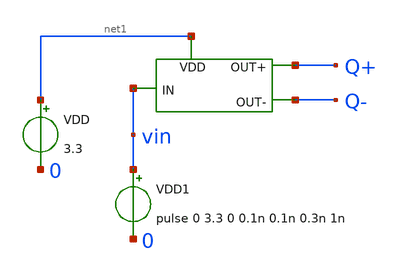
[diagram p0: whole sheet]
** sch_path: initial_notebooks_2023/Current-Steering DAC/DAC/Test_Latch.sch
**.subckt Test_Latch
x1 net1 Q+ vin Q- latch1
VDD net1 0 3.3
VDD1 vin 0 pulse 0 3.3 0 0.1n 0.1n 0.3n 1n
**** begin user architecture code




.include /foss/pdks/gf180mcuC/libs.tech/ngspice/design.ngspice
.lib /foss/pdks/gf180mcuC/libs.tech/ngspice/sm141064.ngspice typical


.control
	tran 1n 10n
	*dc vin1 0 3.3 0.1
	plot v(vin) v(Q-)
	*plot v(vout)
.endc
.save all




**** end user architecture code
**.ends
.end
